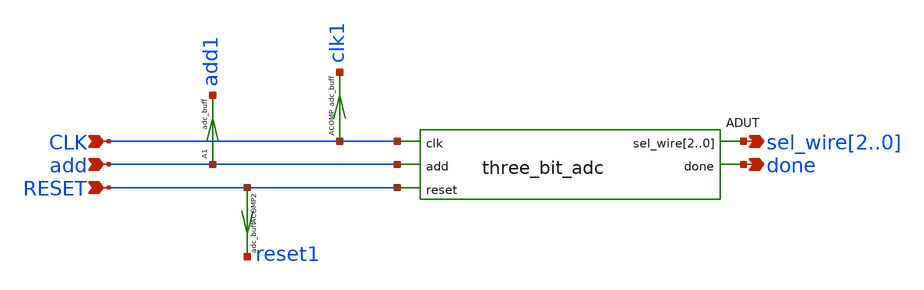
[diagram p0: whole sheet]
** sch_path: 1bit_adc/test_three_bit_adc.sch
**.subckt test_three_bit_adc RESET done add sel_wire2,sel_wire1,sel_wire0 CLK
*.ipin RESET
*.opin done
*.ipin add
*.opin sel_wire2,sel_wire1,sel_wire0
*.ipin CLK
ADUT CLK sel_wire2 sel_wire1 sel_wire0 add RESET done three_bit_adc
ACOMP [ CLK ] [ clk1 ] adc_buff
A1 [ add ] [ add1 ] adc_buff
ACOMP2 [ RESET ] [ reset1 ] adc_buff
**** begin user architecture code


.param vdd=1.8
VVDD VDD 0 DC {vdd}
VCLK CLK 0 PULSE(0 1.8 0   1n 1n 40n 80n)
Vadd add 0 PULSE(0 1.8 0   1n 1n 10n 80n)
VRESET RESET 0 PULSE(0 1.8 0 1n 1n 40n 800n)
VVSS VSS 0 DC 0
.tran 2n 7000n
.control

save all
echo TRAN
run
write 3bit_adc.raw all
.endc
.end




**** end user architecture code
**.ends

* expanding   symbol:  /headless/Documents/1bit_adc/three_bit_adc.sym # of pins=5
** sym_path: 1bit_adc/three_bit_adc.sym
** sch_path: 1bit_adc/three_bit_adc.sch
.subckt three_bit_adc clk sel_wire2 sel_wire1 sel_wire0 add reset done
*.ipin clk
*.ipin reset
*.opin done
*.ipin add
*.opin sel_wire2,sel_wire1,sel_wire0
.ends

**** begin user architecture code
.model adc_buff adc_bridge in_low=0 in_high=1.1
.model three_bit_Adc d_cosim simulation="./three_bit_adc.so"
**** end user architecture code
.end
